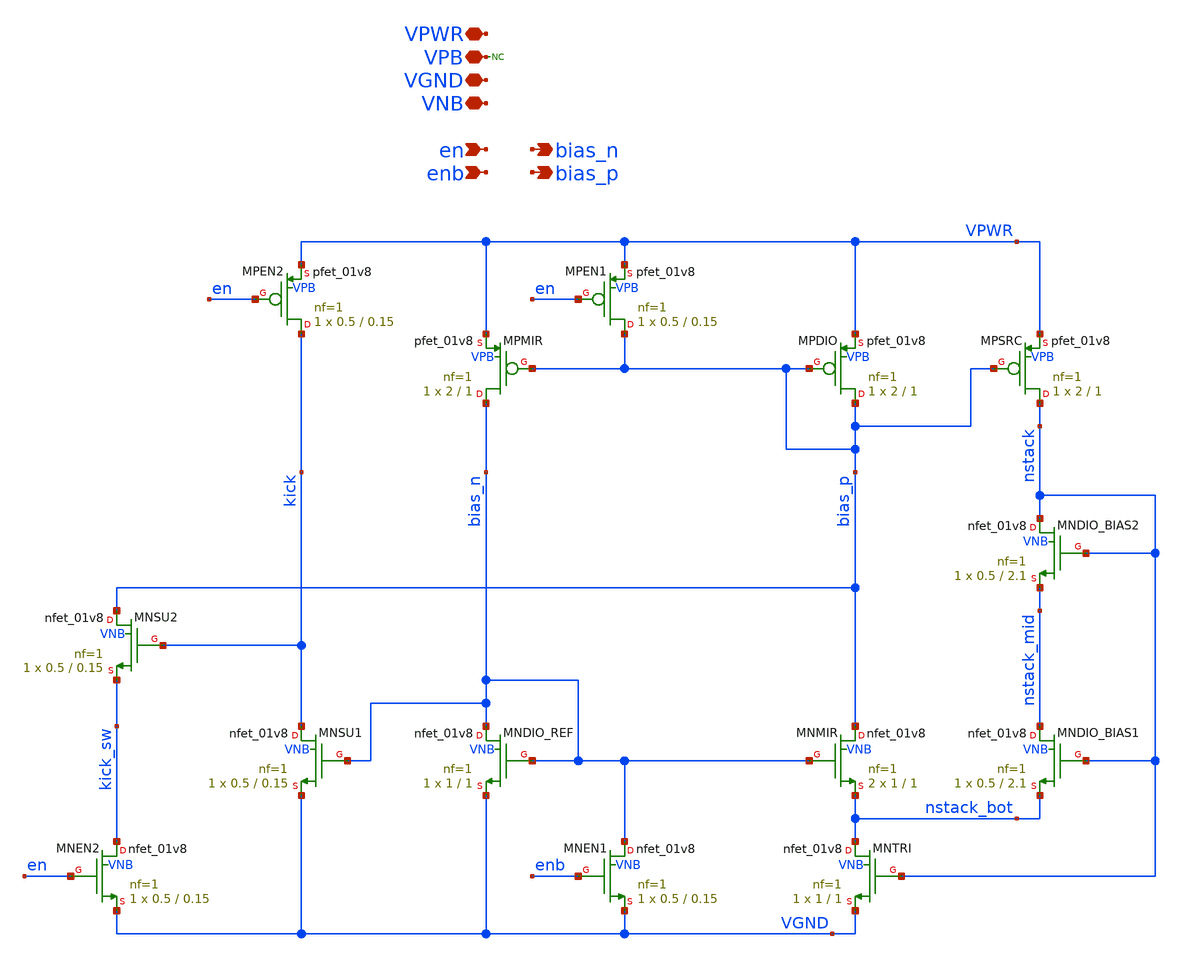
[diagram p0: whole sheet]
** sch_path: xschem/tiny_adc/tiny_adc_bias_gen.sch
**.subckt tiny_adc_bias_gen VNB VGND VPB VPWR bias_n enb en bias_p
*.iopin VNB
*.iopin VGND
*.iopin VPB
*.iopin VPWR
*.opin bias_n
*.ipin enb
*.ipin en
*.opin bias_p
XMNMIR bias_p bias_n nstack_bot VNB sky130_fd_pr__nfet_01v8 L=1 W=1 nf=1 ad='int((nf+1)/2) * W/nf * 0.29'
+ as='int((nf+2)/2) * W/nf * 0.29' pd='2*int((nf+1)/2) * (W/nf + 0.29)' ps='2*int((nf+2)/2) * (W/nf + 0.29)'
+ nrd='0.29 / W' nrs='0.29 / W' sa=0 sb=0 sd=0 mult=2 m=2
XMNDIO_REF bias_n bias_n VGND VNB sky130_fd_pr__nfet_01v8 L=1 W=1 nf=1 ad='int((nf+1)/2) * W/nf * 0.29'
+ as='int((nf+2)/2) * W/nf * 0.29' pd='2*int((nf+1)/2) * (W/nf + 0.29)' ps='2*int((nf+2)/2) * (W/nf + 0.29)'
+ nrd='0.29 / W' nrs='0.29 / W' sa=0 sb=0 sd=0 mult=1 m=1
XMPDIO bias_p bias_p VPWR VPB sky130_fd_pr__pfet_01v8 L=1 W=2 nf=1 ad='int((nf+1)/2) * W/nf * 0.29' as='int((nf+2)/2) * W/nf * 0.29'
+ pd='2*int((nf+1)/2) * (W/nf + 0.29)' ps='2*int((nf+2)/2) * (W/nf + 0.29)' nrd='0.29 / W' nrs='0.29 / W'
+ sa=0 sb=0 sd=0 mult=1 m=1
XMPMIR bias_n bias_p VPWR VPB sky130_fd_pr__pfet_01v8 L=1 W=2 nf=1 ad='int((nf+1)/2) * W/nf * 0.29' as='int((nf+2)/2) * W/nf * 0.29'
+ pd='2*int((nf+1)/2) * (W/nf + 0.29)' ps='2*int((nf+2)/2) * (W/nf + 0.29)' nrd='0.29 / W' nrs='0.29 / W'
+ sa=0 sb=0 sd=0 mult=1 m=1
* noconn VPB
XMNEN1 bias_n enb VGND VNB sky130_fd_pr__nfet_01v8 L=0.15 W=0.5 nf=1 ad='int((nf+1)/2) * W/nf * 0.29'
+ as='int((nf+2)/2) * W/nf * 0.29' pd='2*int((nf+1)/2) * (W/nf + 0.29)' ps='2*int((nf+2)/2) * (W/nf + 0.29)'
+ nrd='0.29 / W' nrs='0.29 / W' sa=0 sb=0 sd=0 mult=1 m=1
XMPEN1 bias_p en VPWR VPB sky130_fd_pr__pfet_01v8 L=0.15 W=0.5 nf=1 ad='int((nf+1)/2) * W/nf * 0.29'
+ as='int((nf+2)/2) * W/nf * 0.29' pd='2*int((nf+1)/2) * (W/nf + 0.29)' ps='2*int((nf+2)/2) * (W/nf + 0.29)'
+ nrd='0.29 / W' nrs='0.29 / W' sa=0 sb=0 sd=0 mult=1 m=1
XMNSU1 kick bias_n VGND VNB sky130_fd_pr__nfet_01v8 L=0.15 W=0.5 nf=1 ad='int((nf+1)/2) * W/nf * 0.29'
+ as='int((nf+2)/2) * W/nf * 0.29' pd='2*int((nf+1)/2) * (W/nf + 0.29)' ps='2*int((nf+2)/2) * (W/nf + 0.29)'
+ nrd='0.29 / W' nrs='0.29 / W' sa=0 sb=0 sd=0 mult=1 m=1
XMNSU2 bias_p kick kick_sw VNB sky130_fd_pr__nfet_01v8 L=0.15 W=0.5 nf=1 ad='int((nf+1)/2) * W/nf * 0.29'
+ as='int((nf+2)/2) * W/nf * 0.29' pd='2*int((nf+1)/2) * (W/nf + 0.29)' ps='2*int((nf+2)/2) * (W/nf + 0.29)'
+ nrd='0.29 / W' nrs='0.29 / W' sa=0 sb=0 sd=0 mult=1 m=1
XMNEN2 kick_sw en VGND VNB sky130_fd_pr__nfet_01v8 L=0.15 W=0.5 nf=1 ad='int((nf+1)/2) * W/nf * 0.29'
+ as='int((nf+2)/2) * W/nf * 0.29' pd='2*int((nf+1)/2) * (W/nf + 0.29)' ps='2*int((nf+2)/2) * (W/nf + 0.29)'
+ nrd='0.29 / W' nrs='0.29 / W' sa=0 sb=0 sd=0 mult=1 m=1
XMPEN2 kick en VPWR VPB sky130_fd_pr__pfet_01v8 L=0.15 W=0.5 nf=1 ad='int((nf+1)/2) * W/nf * 0.29' as='int((nf+2)/2) * W/nf * 0.29'
+ pd='2*int((nf+1)/2) * (W/nf + 0.29)' ps='2*int((nf+2)/2) * (W/nf + 0.29)' nrd='0.29 / W' nrs='0.29 / W'
+ sa=0 sb=0 sd=0 mult=1 m=1
XMNTRI nstack_bot nstack VGND VNB sky130_fd_pr__nfet_01v8 L=1 W=1 nf=1 ad='int((nf+1)/2) * W/nf * 0.29'
+ as='int((nf+2)/2) * W/nf * 0.29' pd='2*int((nf+1)/2) * (W/nf + 0.29)' ps='2*int((nf+2)/2) * (W/nf + 0.29)'
+ nrd='0.29 / W' nrs='0.29 / W' sa=0 sb=0 sd=0 mult=1 m=1
XMPSRC nstack bias_p VPWR VPB sky130_fd_pr__pfet_01v8 L=1 W=2 nf=1 ad='int((nf+1)/2) * W/nf * 0.29' as='int((nf+2)/2) * W/nf * 0.29'
+ pd='2*int((nf+1)/2) * (W/nf + 0.29)' ps='2*int((nf+2)/2) * (W/nf + 0.29)' nrd='0.29 / W' nrs='0.29 / W'
+ sa=0 sb=0 sd=0 mult=1 m=1
XMNDIO_BIAS2 nstack nstack nstack_mid VNB sky130_fd_pr__nfet_01v8 L=2.1 W=0.5 nf=1 ad='int((nf+1)/2) * W/nf * 0.29'
+ as='int((nf+2)/2) * W/nf * 0.29' pd='2*int((nf+1)/2) * (W/nf + 0.29)' ps='2*int((nf+2)/2) * (W/nf + 0.29)'
+ nrd='0.29 / W' nrs='0.29 / W' sa=0 sb=0 sd=0 mult=1 m=1
XMNDIO_BIAS1 nstack_mid nstack nstack_bot VNB sky130_fd_pr__nfet_01v8 L=2.1 W=0.5 nf=1 ad='int((nf+1)/2) * W/nf * 0.29'
+ as='int((nf+2)/2) * W/nf * 0.29' pd='2*int((nf+1)/2) * (W/nf + 0.29)' ps='2*int((nf+2)/2) * (W/nf + 0.29)'
+ nrd='0.29 / W' nrs='0.29 / W' sa=0 sb=0 sd=0 mult=1 m=1
**.ends
.end
